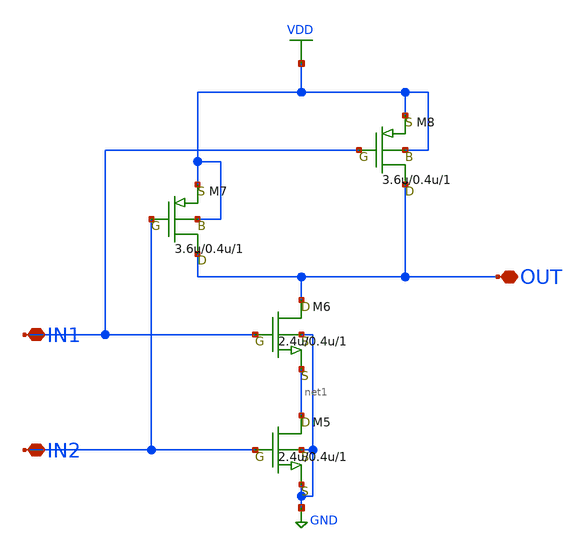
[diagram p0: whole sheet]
** sch_path: LR_hasegawa/LR_Work2/Citizen035/NAND2_Citizen.sch
**.subckt NAND2_Citizen OUT IN1 IN2
*.iopin OUT
*.iopin IN1
*.iopin IN2
M5 net1 IN2 GND GND nch w=2.4u l=0.4u as=0 ps=0 ad=0 pd=0 m=1
M6 OUT IN1 net1 GND nch w=2.4u l=0.4u as=0 ps=0 ad=0 pd=0 m=1
M7 OUT IN2 VDD VDD pch w=3.6u l=0.4u as=0 ps=0 ad=0 pd=0 m=1
M8 OUT IN1 VDD VDD pch w=3.6u l=0.4u as=0 ps=0 ad=0 pd=0 m=1
**.ends
.GLOBAL VDD
.GLOBAL GND
.end
